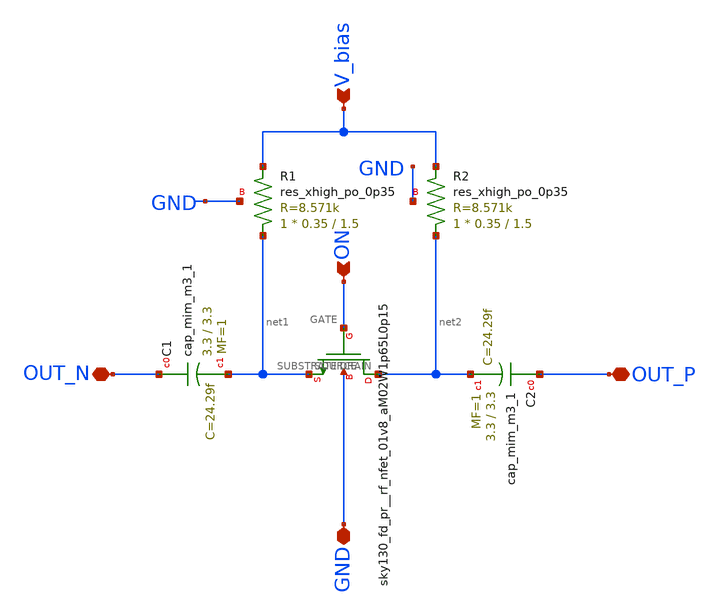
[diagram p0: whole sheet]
** sch_path: xschem/cell_unit.sch
**.subckt cell_unit OUT_N OUT_P GND ON V_bias
*.iopin OUT_N
*.iopin OUT_P
*.iopin GND
*.ipin ON
*.ipin V_bias
XC1 OUT_N net1 sky130_fd_pr__cap_mim_m3_1 W=3.3 L=3.3 MF=1 m=1
XC2 OUT_P net2 sky130_fd_pr__cap_mim_m3_1 W=3.3 L=3.3 MF=1 m=1
XR1 net1 V_bias GND sky130_fd_pr__res_xhigh_po_0p35 L=1.5 mult=1 m=1
XR2 net2 V_bias GND sky130_fd_pr__res_xhigh_po_0p35 L=1.5 mult=1 m=1
X1 sky130_fd_pr__rf_nfet_01v8_aM02W1p65L0p15 net2 ON net1 GND
**.ends

* expanding   symbol:  sky130_fd_pr__rf_nfet_01v8_aM02W1p65L0p15.sym # of pins=4
** sym_path: xschem/sky130_fd_pr__rf_nfet_01v8_aM02W1p65L0p15.sym
** sch_path: xschem/sky130_fd_pr__rf_nfet_01v8_aM02W1p65L0p15.sch
.subckt sky130_fd_pr__rf_nfet_01v8_aM02W1p65L0p15
*.iopin SOURCE
*.iopin DRAIN
*.ipin SUBSTRATE
*.ipin GATE
**** begin user architecture code


.subckt sky130_fd_pr__rf_nfet_01v8_aM02W1p65L0p15 DRAIN GATE SOURCE SUBSTRATE
X0 SOURCE GATE DRAIN SUBSTRATE sky130_fd_pr__nfet_01v8 w=1.65e+06u l=150000u
X1 DRAIN GATE SOURCE SUBSTRATE sky130_fd_pr__nfet_01v8 w=1.65e+06u l=150000u
.ends

**** end user architecture code
.ends

.end
